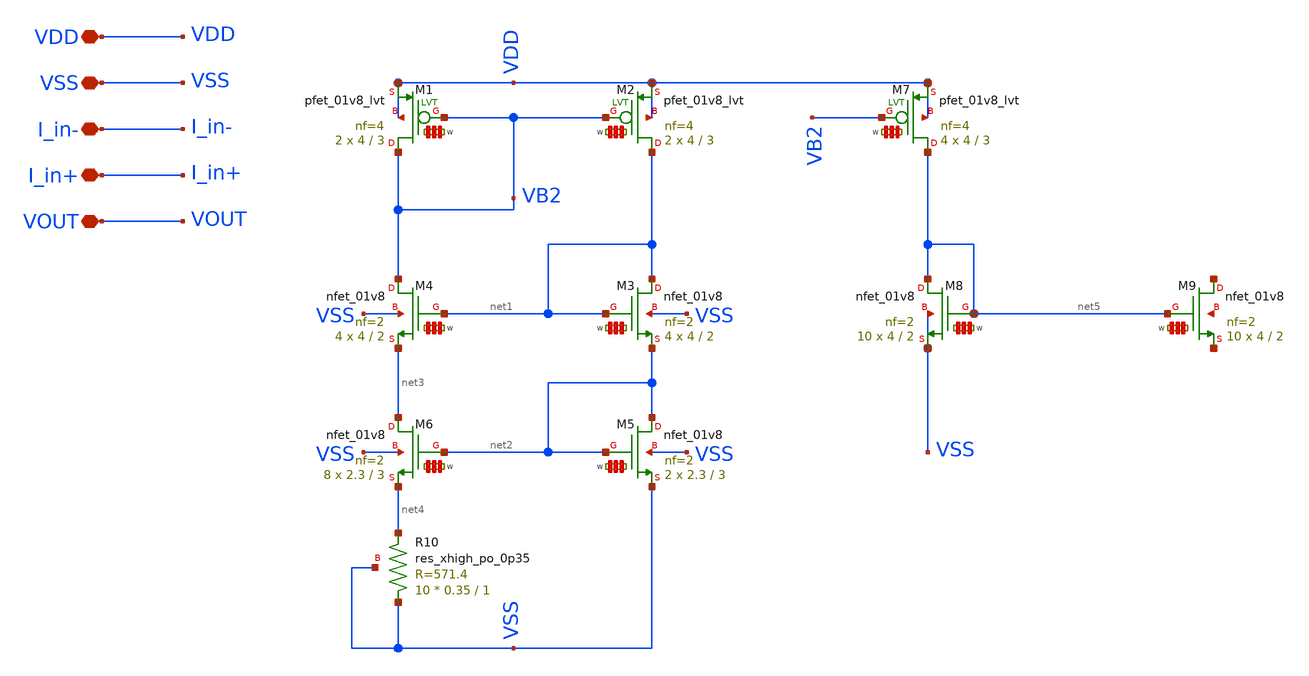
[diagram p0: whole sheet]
** sch_path: my_ip/sky130A/OTRA_VGA/OTRA.sch
**.subckt OTRA VDD VSS I_in- I_in+ VOUT
*.iopin VDD
*.iopin VSS
*.iopin I_in-
*.iopin I_in+
*.iopin VOUT
XM2 net1 VB2 VDD VDD sky130_fd_pr__pfet_01v8_lvt L=3 W='4 * 4 ' nf=4 ad='int((4 + 1)/2) * 4 / 4 * 0.29'
+ as='int((4 + 2)/2) * 4 / 4 * 0.29' pd='2*int((4 + 1)/2) * (4 / 4 + 0.29)' ps='2*int((4 + 2)/2) * (4 / 4 + 0.29)'
+ nrd='0.29 / 4 ' nrs='0.29 / 4 ' sa=0 sb=0 sd=0 mult=2 m=2
XM1 VB2 VB2 VDD VDD sky130_fd_pr__pfet_01v8_lvt L=3 W='4 * 4 ' nf=4 ad='int((4 + 1)/2) * 4 / 4 * 0.29'
+ as='int((4 + 2)/2) * 4 / 4 * 0.29' pd='2*int((4 + 1)/2) * (4 / 4 + 0.29)' ps='2*int((4 + 2)/2) * (4 / 4 + 0.29)'
+ nrd='0.29 / 4 ' nrs='0.29 / 4 ' sa=0 sb=0 sd=0 mult=2 m=2
XR10 VSS net4 VSS sky130_fd_pr__res_xhigh_po_0p35 L=1 mult=10 m=10
XM4 VB2 net1 net3 VSS sky130_fd_pr__nfet_01v8 L=2 W='4 * 2 ' nf=2 ad='int((2 + 1)/2) * 4 / 2 * 0.29'
+ as='int((2 + 2)/2) * 4 / 2 * 0.29' pd='2*int((2 + 1)/2) * (4 / 2 + 0.29)' ps='2*int((2 + 2)/2) * (4 / 2 + 0.29)'
+ nrd='0.29 / 4 ' nrs='0.29 / 4 ' sa=0 sb=0 sd=0 mult=4 m=4
XM3 net1 net1 net2 VSS sky130_fd_pr__nfet_01v8 L=2 W='4 * 2 ' nf=2 ad='int((2 + 1)/2) * 4 / 2 * 0.29'
+ as='int((2 + 2)/2) * 4 / 2 * 0.29' pd='2*int((2 + 1)/2) * (4 / 2 + 0.29)' ps='2*int((2 + 2)/2) * (4 / 2 + 0.29)'
+ nrd='0.29 / 4 ' nrs='0.29 / 4 ' sa=0 sb=0 sd=0 mult=4 m=4
XM6 net3 net2 net4 VSS sky130_fd_pr__nfet_01v8 L=3 W='2.3 * 2 ' nf=2 ad='int((2 + 1)/2) * 2.3 / 2 * 0.29'
+ as='int((2 + 2)/2) * 2.3 / 2 * 0.29' pd='2*int((2 + 1)/2) * (2.3 / 2 + 0.29)' ps='2*int((2 + 2)/2) * (2.3 / 2 + 0.29)'
+ nrd='0.29 / 2.3 ' nrs='0.29 / 2.3 ' sa=0 sb=0 sd=0 mult=8 m=8
XM5 net2 net2 VSS VSS sky130_fd_pr__nfet_01v8 L=3 W='2.3 * 2 ' nf=2 ad='int((2 + 1)/2) * 2.3 / 2 * 0.29'
+ as='int((2 + 2)/2) * 2.3 / 2 * 0.29' pd='2*int((2 + 1)/2) * (2.3 / 2 + 0.29)' ps='2*int((2 + 2)/2) * (2.3 / 2 + 0.29)'
+ nrd='0.29 / 2.3 ' nrs='0.29 / 2.3 ' sa=0 sb=0 sd=0 mult=2 m=2
XM7 net5 VB2 VDD VDD sky130_fd_pr__pfet_01v8_lvt L=3 W='4 * 4 ' nf=4 ad='int((4 + 1)/2) * 4 / 4 * 0.29'
+ as='int((4 + 2)/2) * 4 / 4 * 0.29' pd='2*int((4 + 1)/2) * (4 / 4 + 0.29)' ps='2*int((4 + 2)/2) * (4 / 4 + 0.29)'
+ nrd='0.29 / 4 ' nrs='0.29 / 4 ' sa=0 sb=0 sd=0 mult=4 m=4
XM8 net5 net5 VSS VSS sky130_fd_pr__nfet_01v8 L=2 W='4 * 2 ' nf=2 ad='int((2 + 1)/2) * 4 / 2 * 0.29'
+ as='int((2 + 2)/2) * 4 / 2 * 0.29' pd='2*int((2 + 1)/2) * (4 / 2 + 0.29)' ps='2*int((2 + 2)/2) * (4 / 2 + 0.29)'
+ nrd='0.29 / 4 ' nrs='0.29 / 4 ' sa=0 sb=0 sd=0 mult=10 m=10
XM9 net6 net5 net7 net8 sky130_fd_pr__nfet_01v8 L=2 W='4 * 2 ' nf=2 ad='int((2 + 1)/2) * 4 / 2 * 0.29'
+ as='int((2 + 2)/2) * 4 / 2 * 0.29' pd='2*int((2 + 1)/2) * (4 / 2 + 0.29)' ps='2*int((2 + 2)/2) * (4 / 2 + 0.29)'
+ nrd='0.29 / 4 ' nrs='0.29 / 4 ' sa=0 sb=0 sd=0 mult=10 m=10
**.ends
.end
